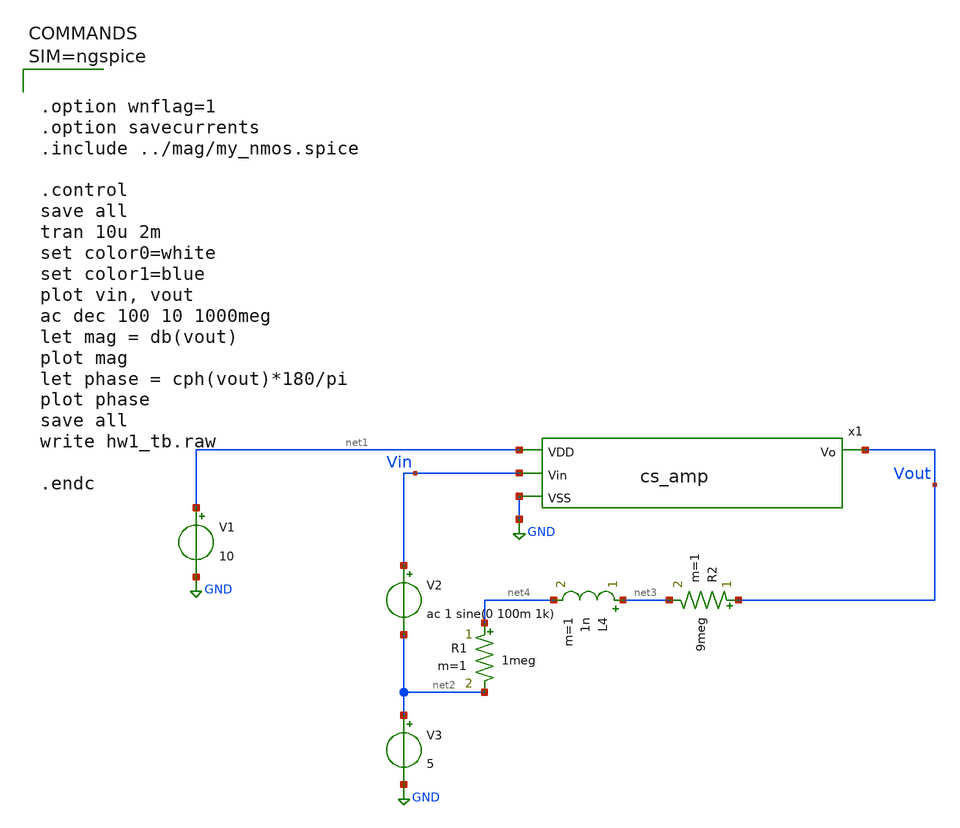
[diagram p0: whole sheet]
** sch_path: hw02/xschem/amp_tb.sch
**.subckt amp_tb
V1 net1 GND 10
V2 Vin net2 ac 1 sine(0 100m 1k)
V3 net2 GND 5
R1 net4 net2 1meg m=1
R2 Vout net3 9meg m=1
L4 net3 net4 1n m=1
x1 net1 Vout Vin GND cs_amp
**** begin user architecture code



.option wnflag=1
.option savecurrents
.include ../mag/my_nmos.spice

.control
save all
tran 10u 2m
set color0=white
set color1=blue
plot vin, vout
ac dec 100 10 1000meg
let mag = db(vout)
plot mag
let phase = cph(vout)*180/pi
plot phase
save all
write hw1_tb.raw

.endc




** opencircuitdesign pdks install
.lib $::SKYWATER_MODELS/sky130.lib.spice tt


**** end user architecture code
**.ends
.GLOBAL GND
.end
